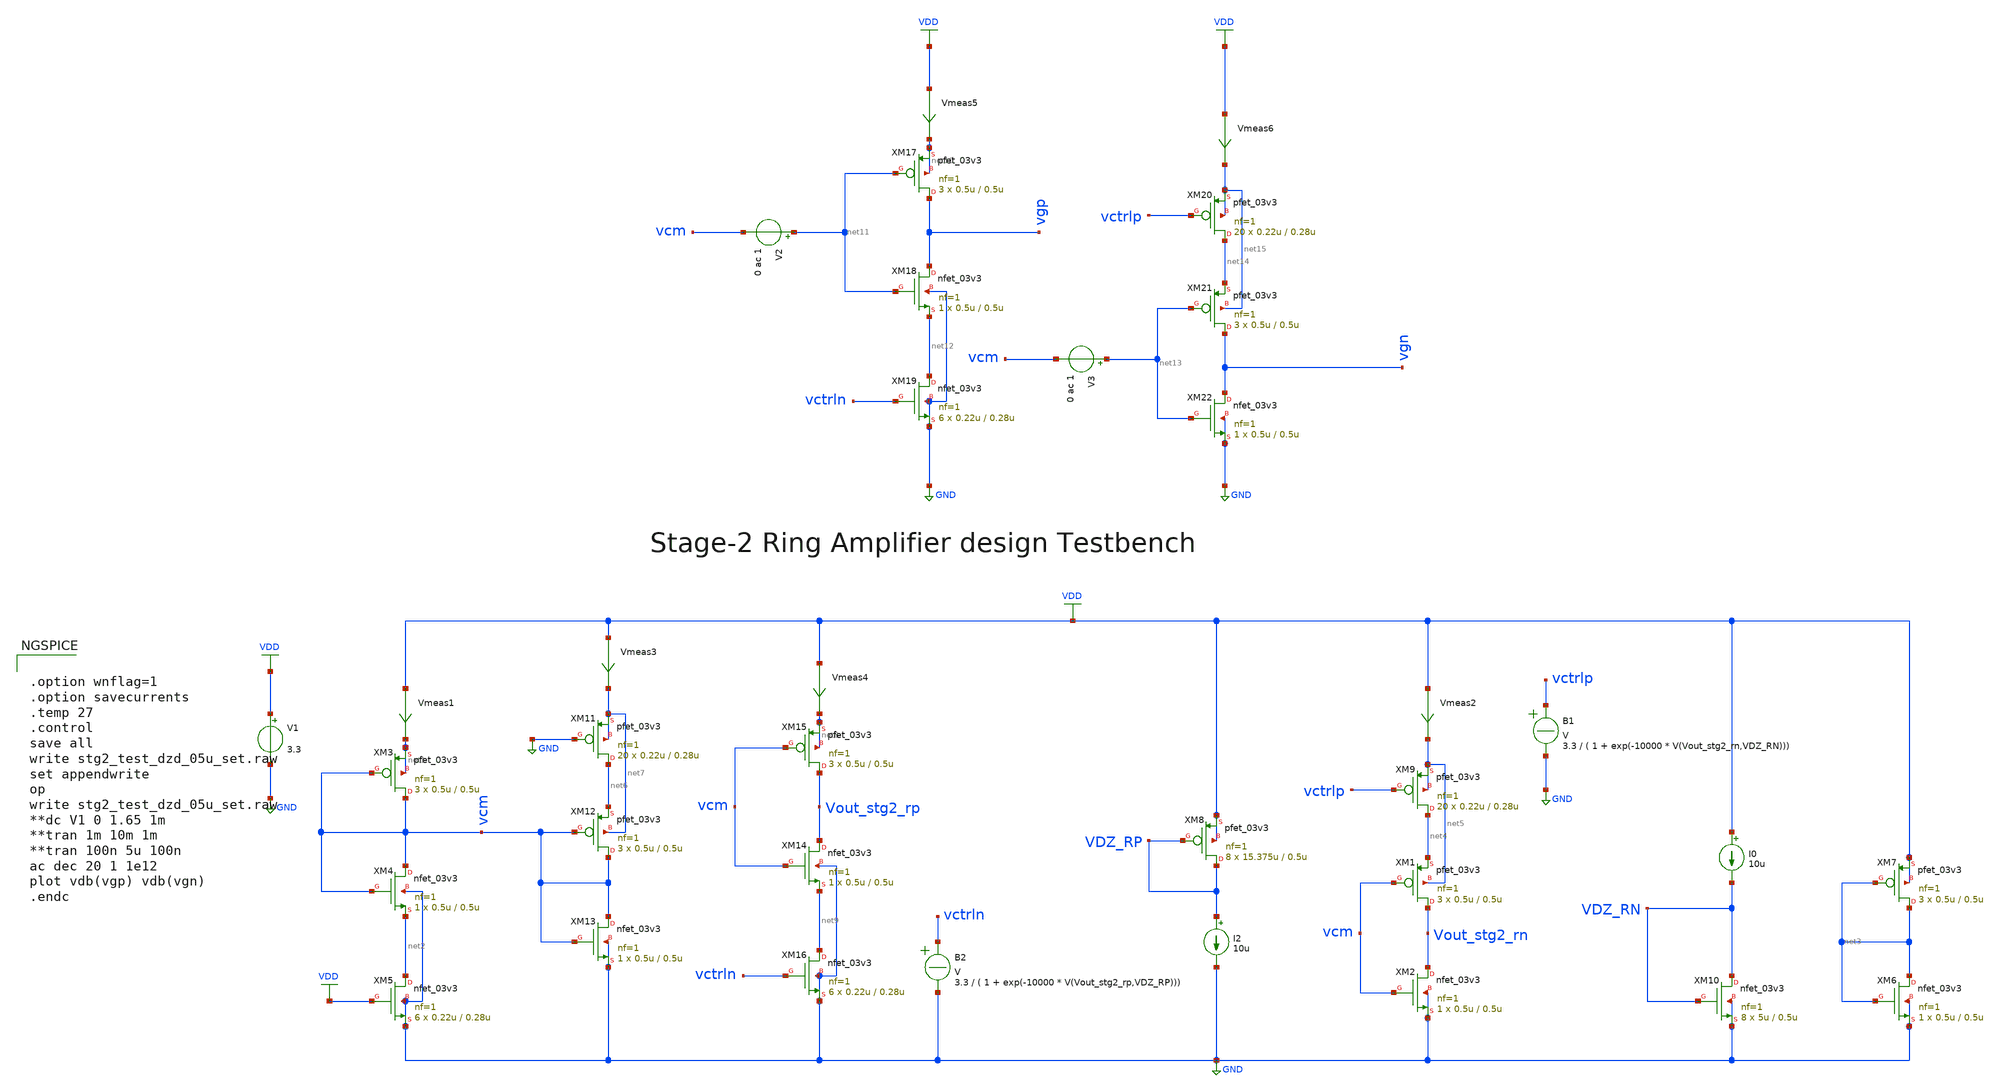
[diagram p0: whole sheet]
** sch_path: Design_Files/Ring-amp/STG2/stg2_test_dzd_05u_set.sch
**.subckt stg2_test_dzd_05u_set
XM6 net3 net3 GND GND nfet_03v3 L=0.5u W=0.5u nf=1 ad='int((nf+1)/2) * W/nf * 0.18u' as='int((nf+2)/2) * W/nf * 0.18u'
+ pd='2*int((nf+1)/2) * (W/nf + 0.18u)' ps='2*int((nf+2)/2) * (W/nf + 0.18u)' nrd='0.18u / W' nrs='0.18u / W'
+ sa=0 sb=0 sd=0 m=1
XM7 net3 net3 VDD VDD pfet_03v3 L=0.5u W=0.5u nf=1 ad='int((nf+1)/2) * W/nf * 0.18u' as='int((nf+2)/2) * W/nf * 0.18u'
+ pd='2*int((nf+1)/2) * (W/nf + 0.18u)' ps='2*int((nf+2)/2) * (W/nf + 0.18u)' nrd='0.18u / W' nrs='0.18u / W'
+ sa=0 sb=0 sd=0 m=3
XM8 VDZ_RP VDZ_RP VDD VDD pfet_03v3 L=0.5u W=15.375u nf=1 ad='int((nf+1)/2) * W/nf * 0.18u' as='int((nf+2)/2) * W/nf * 0.18u'
+ pd='2*int((nf+1)/2) * (W/nf + 0.18u)' ps='2*int((nf+2)/2) * (W/nf + 0.18u)' nrd='0.18u / W' nrs='0.18u / W'
+ sa=0 sb=0 sd=0 m=8
I2 VDZ_RP GND 10u
B2 vctrln GND V = 3.3 / ( 1 + exp(-10000 * V(Vout_stg2_rp,VDZ_RP)))
V1 VDD GND 3.3
Vmeas1 VDD net1 0
.save i(vmeas1)
XM1 Vout_stg2_rn vcm net4 net5 pfet_03v3 L=0.5u W=0.5u nf=1 ad='int((nf+1)/2) * W/nf * 0.18u' as='int((nf+2)/2) * W/nf * 0.18u'
+ pd='2*int((nf+1)/2) * (W/nf + 0.18u)' ps='2*int((nf+2)/2) * (W/nf + 0.18u)' nrd='0.18u / W' nrs='0.18u / W'
+ sa=0 sb=0 sd=0 m=3
XM2 Vout_stg2_rn vcm GND GND nfet_03v3 L=0.5u W=0.5u nf=1 ad='int((nf+1)/2) * W/nf * 0.18u' as='int((nf+2)/2) * W/nf * 0.18u'
+ pd='2*int((nf+1)/2) * (W/nf + 0.18u)' ps='2*int((nf+2)/2) * (W/nf + 0.18u)' nrd='0.18u / W' nrs='0.18u / W'
+ sa=0 sb=0 sd=0 m=1
XM9 net4 vctrlp net5 net5 pfet_03v3 L=0.28u W=0.22u nf=1 ad='int((nf+1)/2) * W/nf * 0.18u' as='int((nf+2)/2) * W/nf * 0.18u'
+ pd='2*int((nf+1)/2) * (W/nf + 0.18u)' ps='2*int((nf+2)/2) * (W/nf + 0.18u)' nrd='0.18u / W' nrs='0.18u / W'
+ sa=0 sb=0 sd=0 m=20
Vmeas2 VDD net5 0
.save i(vmeas2)
XM10 VDZ_RN VDZ_RN GND GND nfet_03v3 L=0.5u W=5u nf=1 ad='int((nf+1)/2) * W/nf * 0.18u' as='int((nf+2)/2) * W/nf * 0.18u'
+ pd='2*int((nf+1)/2) * (W/nf + 0.18u)' ps='2*int((nf+2)/2) * (W/nf + 0.18u)' nrd='0.18u / W' nrs='0.18u / W'
+ sa=0 sb=0 sd=0 m=8
I0 VDD VDZ_RN 10u
B1 vctrlp GND V = 3.3 / ( 1 + exp(-10000 * V(Vout_stg2_rn,VDZ_RN)))
Vmeas3 VDD net7 0
.save i(vmeas3)
XM14 Vout_stg2_rp vcm net9 GND nfet_03v3 L=0.5u W=0.5u nf=1 ad='int((nf+1)/2) * W/nf * 0.18u' as='int((nf+2)/2) * W/nf * 0.18u'
+ pd='2*int((nf+1)/2) * (W/nf + 0.18u)' ps='2*int((nf+2)/2) * (W/nf + 0.18u)' nrd='0.18u / W' nrs='0.18u / W'
+ sa=0 sb=0 sd=0 m=1
XM15 Vout_stg2_rp vcm net8 net8 pfet_03v3 L=0.5u W=0.5u nf=1 ad='int((nf+1)/2) * W/nf * 0.18u' as='int((nf+2)/2) * W/nf * 0.18u'
+ pd='2*int((nf+1)/2) * (W/nf + 0.18u)' ps='2*int((nf+2)/2) * (W/nf + 0.18u)' nrd='0.18u / W' nrs='0.18u / W'
+ sa=0 sb=0 sd=0 m=3
XM16 net9 vctrln GND GND nfet_03v3 L=0.28u W=0.22u nf=1 ad='int((nf+1)/2) * W/nf * 0.18u' as='int((nf+2)/2) * W/nf * 0.18u'
+ pd='2*int((nf+1)/2) * (W/nf + 0.18u)' ps='2*int((nf+2)/2) * (W/nf + 0.18u)' nrd='0.18u / W' nrs='0.18u / W'
+ sa=0 sb=0 sd=0 m=6
Vmeas4 VDD net8 0
.save i(vmeas4)
Vmeas5 VDD net10 0
.save i(vmeas5)
V2 net11 vcm 0 ac 1
Vmeas6 VDD net15 0
.save i(vmeas6)
V3 net13 vcm 0 ac 1
XM3 vcm vcm net1 net1 pfet_03v3 L=0.5u W=0.5u nf=1 ad='int((nf+1)/2) * W/nf * 0.18u' as='int((nf+2)/2) * W/nf * 0.18u'
+ pd='2*int((nf+1)/2) * (W/nf + 0.18u)' ps='2*int((nf+2)/2) * (W/nf + 0.18u)' nrd='0.18u / W' nrs='0.18u / W'
+ sa=0 sb=0 sd=0 m=3
XM4 vcm vcm net2 GND nfet_03v3 L=0.5u W=0.5u nf=1 ad='int((nf+1)/2) * W/nf * 0.18u' as='int((nf+2)/2) * W/nf * 0.18u'
+ pd='2*int((nf+1)/2) * (W/nf + 0.18u)' ps='2*int((nf+2)/2) * (W/nf + 0.18u)' nrd='0.18u / W' nrs='0.18u / W'
+ sa=0 sb=0 sd=0 m=1
XM5 net2 VDD GND GND nfet_03v3 L=0.28u W=0.22u nf=1 ad='int((nf+1)/2) * W/nf * 0.18u' as='int((nf+2)/2) * W/nf * 0.18u'
+ pd='2*int((nf+1)/2) * (W/nf + 0.18u)' ps='2*int((nf+2)/2) * (W/nf + 0.18u)' nrd='0.18u / W' nrs='0.18u / W'
+ sa=0 sb=0 sd=0 m=6
XM11 net6 GND net7 net7 pfet_03v3 L=0.28u W=0.22u nf=1 ad='int((nf+1)/2) * W/nf * 0.18u' as='int((nf+2)/2) * W/nf * 0.18u'
+ pd='2*int((nf+1)/2) * (W/nf + 0.18u)' ps='2*int((nf+2)/2) * (W/nf + 0.18u)' nrd='0.18u / W' nrs='0.18u / W'
+ sa=0 sb=0 sd=0 m=20
XM12 vcm vcm net6 net7 pfet_03v3 L=0.5u W=0.5u nf=1 ad='int((nf+1)/2) * W/nf * 0.18u' as='int((nf+2)/2) * W/nf * 0.18u'
+ pd='2*int((nf+1)/2) * (W/nf + 0.18u)' ps='2*int((nf+2)/2) * (W/nf + 0.18u)' nrd='0.18u / W' nrs='0.18u / W'
+ sa=0 sb=0 sd=0 m=3
XM13 vcm vcm GND GND nfet_03v3 L=0.5u W=0.5u nf=1 ad='int((nf+1)/2) * W/nf * 0.18u' as='int((nf+2)/2) * W/nf * 0.18u'
+ pd='2*int((nf+1)/2) * (W/nf + 0.18u)' ps='2*int((nf+2)/2) * (W/nf + 0.18u)' nrd='0.18u / W' nrs='0.18u / W'
+ sa=0 sb=0 sd=0 m=1
XM17 vgp net11 net10 net10 pfet_03v3 L=0.5u W=0.5u nf=1 ad='int((nf+1)/2) * W/nf * 0.18u' as='int((nf+2)/2) * W/nf * 0.18u'
+ pd='2*int((nf+1)/2) * (W/nf + 0.18u)' ps='2*int((nf+2)/2) * (W/nf + 0.18u)' nrd='0.18u / W' nrs='0.18u / W'
+ sa=0 sb=0 sd=0 m=3
XM18 vgp net11 net12 GND nfet_03v3 L=0.5u W=0.5u nf=1 ad='int((nf+1)/2) * W/nf * 0.18u' as='int((nf+2)/2) * W/nf * 0.18u'
+ pd='2*int((nf+1)/2) * (W/nf + 0.18u)' ps='2*int((nf+2)/2) * (W/nf + 0.18u)' nrd='0.18u / W' nrs='0.18u / W'
+ sa=0 sb=0 sd=0 m=1
XM19 net12 vctrln GND GND nfet_03v3 L=0.28u W=0.22u nf=1 ad='int((nf+1)/2) * W/nf * 0.18u' as='int((nf+2)/2) * W/nf * 0.18u'
+ pd='2*int((nf+1)/2) * (W/nf + 0.18u)' ps='2*int((nf+2)/2) * (W/nf + 0.18u)' nrd='0.18u / W' nrs='0.18u / W'
+ sa=0 sb=0 sd=0 m=6
XM20 net14 vctrlp net15 net15 pfet_03v3 L=0.28u W=0.22u nf=1 ad='int((nf+1)/2) * W/nf * 0.18u' as='int((nf+2)/2) * W/nf * 0.18u'
+ pd='2*int((nf+1)/2) * (W/nf + 0.18u)' ps='2*int((nf+2)/2) * (W/nf + 0.18u)' nrd='0.18u / W' nrs='0.18u / W'
+ sa=0 sb=0 sd=0 m=20
XM21 vgn net13 net14 net15 pfet_03v3 L=0.5u W=0.5u nf=1 ad='int((nf+1)/2) * W/nf * 0.18u' as='int((nf+2)/2) * W/nf * 0.18u'
+ pd='2*int((nf+1)/2) * (W/nf + 0.18u)' ps='2*int((nf+2)/2) * (W/nf + 0.18u)' nrd='0.18u / W' nrs='0.18u / W'
+ sa=0 sb=0 sd=0 m=3
XM22 vgn net13 GND GND nfet_03v3 L=0.5u W=0.5u nf=1 ad='int((nf+1)/2) * W/nf * 0.18u' as='int((nf+2)/2) * W/nf * 0.18u'
+ pd='2*int((nf+1)/2) * (W/nf + 0.18u)' ps='2*int((nf+2)/2) * (W/nf + 0.18u)' nrd='0.18u / W' nrs='0.18u / W'
+ sa=0 sb=0 sd=0 m=1
**** begin user architecture code


.option wnflag=1
.option savecurrents
.temp 27
.control
save all
write stg2_test_dzd_05u_set.raw
set appendwrite
op
write stg2_test_dzd_05u_set.raw
**dc V1 0 1.65 1m
**tran 1m 10m 1m
**tran 100n 5u 100n
ac dec 20 1 1e12
plot vdb(vgp) vdb(vgn)
.endc



.lib /foss/pdks/volare/gf180mcu/versions/0fe599b2afb6708d281543108caf8310912f54af/gf180mcuD/libs.tech/ngspice/sm141064.ngspice typical
.include /foss/pdks/volare/gf180mcu/versions/0fe599b2afb6708d281543108caf8310912f54af/gf180mcuD/libs.tech/ngspice/design.ngspice
.lib /foss/pdks/volare/gf180mcu/versions/0fe599b2afb6708d281543108caf8310912f54af/gf180mcuD/libs.tech/ngspice/sm141064.ngspice res_statistical

**.include $::180MCU_MODELS/design.ngspice
**.lib $::180MCU_MODELS/sm141064.ngspice typical
**.lib $::180MCU_MODELS/sm141064.ngspice res_typical
* .lib $::180MCU_MODELS/sm141064.ngspice res_statistical
*.include $::180MCU_MODELS/design.ngspice
*.lib $::180MCU_MODELS/sm141064.ngspice typical




.save @m.xm1.m0[gm]
.save @m.xm1.m0[id]
.save @m.xm1.m0[vth]
.save @m.xm1.m0[gds]
.save @m.xm1.m0[cgg]
.save @m.xm1.m0[cgs]
.save @m.xm1.m0[cgd]
.save @m.xm2.m0[gm]
.save @m.xm2.m0[id]
.save @m.xm2.m0[vth]
.save @m.xm2.m0[gds]
.save @m.xm2.m0[cgg]
.save @m.xm2.m0[cgs]
.save @m.xm2.m0[cgd]
.save @m.xm3.m0[gm]
.save @m.xm3.m0[id]
.save @m.xm3.m0[vth]
.save @m.xm3.m0[vds]
.save @m.xm3.m0[gds]
.save @m.xm3.m0[cgg]
.save @m.xm3.m0[cgs]
.save @m.xm3.m0[cgd]
.save @m.xm4.m0[gm]
.save @m.xm4.m0[id]
.save @m.xm4.m0[vth]
.save @m.xm4.m0[vds]
.save @m.xm4.m0[gds]
.save @m.xm4.m0[cgg]
.save @m.xm4.m0[cgs]
.save @m.xm4.m0[cgd]


**** end user architecture code
**.ends
.GLOBAL GND
.GLOBAL VDD
.end
